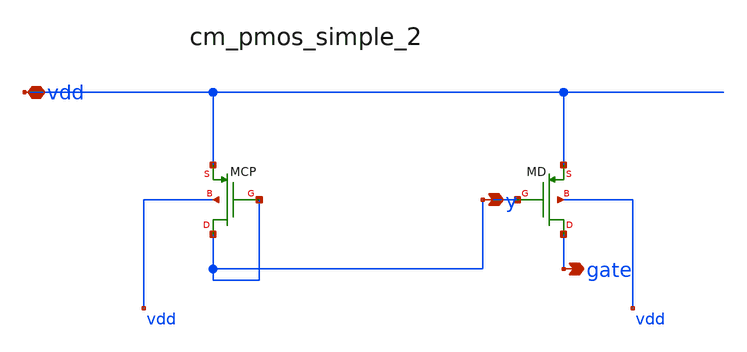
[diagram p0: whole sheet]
** sch_path: analog-db/raw/ldo_010_capless_lowiq/hier/blocks/cm_pmos_simple_2.sch
**.subckt cm_pmos_simple_2 vdd y gate
*.iopin vdd
*.opin y
*.opin gate
XMCP y y vdd vdd sg13_lv_pmos w=x_dut_xmcp_w l=x_dut_xmcp_l ng=1 m=1
XMD gate y vdd vdd sg13_lv_pmos w=x_dut_xmcp_w l=x_dut_xmcp_l ng=1 m=1
**.ends
.end
